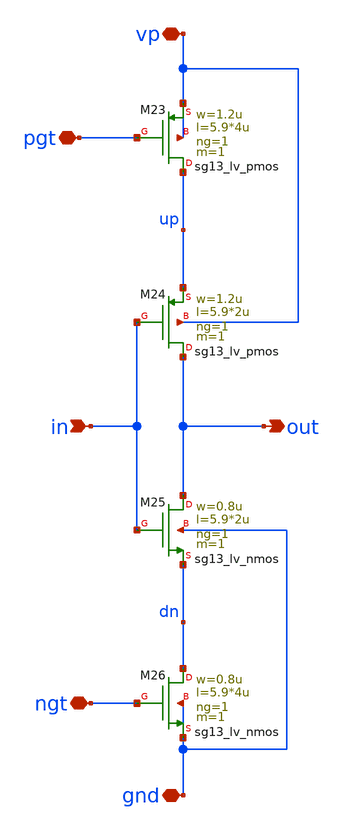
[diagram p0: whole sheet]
** sch_path: PLL0663-main/schematic/xschem/vco/vco_delay_cell_4.sch
**.subckt vco_delay_cell_4 in out gnd vp pgt ngt
*.ipin in
*.opin out
*.iopin gnd
*.iopin vp
*.iopin pgt
*.iopin ngt
XM23 up pgt vp vp sg13_lv_pmos w=1.2u l=5.9*4u ng=1 m=1 mm_ok=1
XM24 out in up vp sg13_lv_pmos w=1.2u l=5.9*2u ng=1 m=1 mm_ok=1
XM25 out in dn gnd sg13_lv_nmos w=0.8u l=5.9*2u ng=1 m=1 mm_ok=1
XM26 dn ngt gnd gnd sg13_lv_nmos w=0.8u l=5.9*4u ng=1 m=1 mm_ok=1
**.ends
.end
